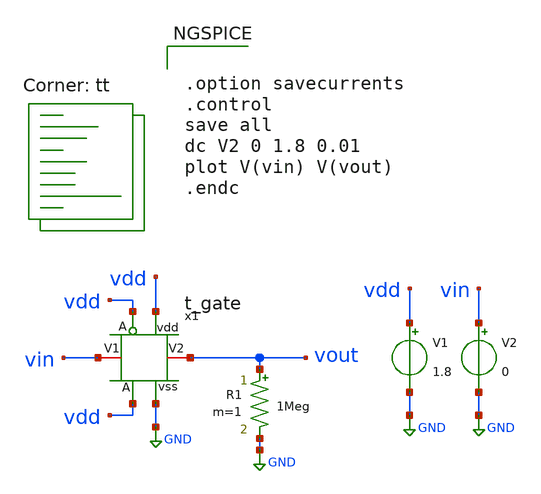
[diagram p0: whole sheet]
** sch_path: xschem/t-gate/t_gate_tb.sch
**.subckt t_gate_tb
x1 vdd vdd vin vout GND t_gate
V1 vdd GND 1.8
V2 vin GND 0
R1 vout GND 1Meg m=1
**** begin user architecture code
.lib $::SKYWATER_MODELS/sky130.lib.spice tt


.option savecurrents
.control
save all
dc V2 0 1.8 0.01
plot V(vin) V(vout)
.endc


**** end user architecture code
**.ends

* expanding   symbol:  t_gate.sym # of pins=6
** sym_path: xschem/t-gate/t_gate.sym
** sch_path: xschem/t-gate/t_gate.sch
.subckt t_gate A vdd V1 V2 vss
*.iopin V1
*.iopin V2
*.ipin A
*.ipin vdd
*.ipin vss
XM2 V1 A V2 vss sky130_fd_pr__nfet_01v8 L=0.17 W=1 nf=1 ad={int((nf+1)/2) * W/nf * 0.29} as={int((nf+2)/2) * W/nf * 0.29}
+ pd={2*int((nf+1)/2) * (W/nf + 0.29)} ps={2*int((nf+2)/2) * (W/nf + 0.29)} nrd={0.29 / W} nrs={0.29 / W}
+ sa=0 sb=0 sd=0 mult=1 m=1
XM1 V1 net1 V2 vdd sky130_fd_pr__pfet_01v8 L=0.17 W=1 nf=1 ad={int((nf+1)/2) * W/nf * 0.29} as={int((nf+2)/2) * W/nf * 0.29}
+ pd={2*int((nf+1)/2) * (W/nf + 0.29)} ps={2*int((nf+2)/2) * (W/nf + 0.29)} nrd={0.29 / W} nrs={0.29 / W}
+ sa=0 sb=0 sd=0 mult=1 m=1
x1 vdd net1 A vss inv_x1
.ends

.GLOBAL GND
.end
